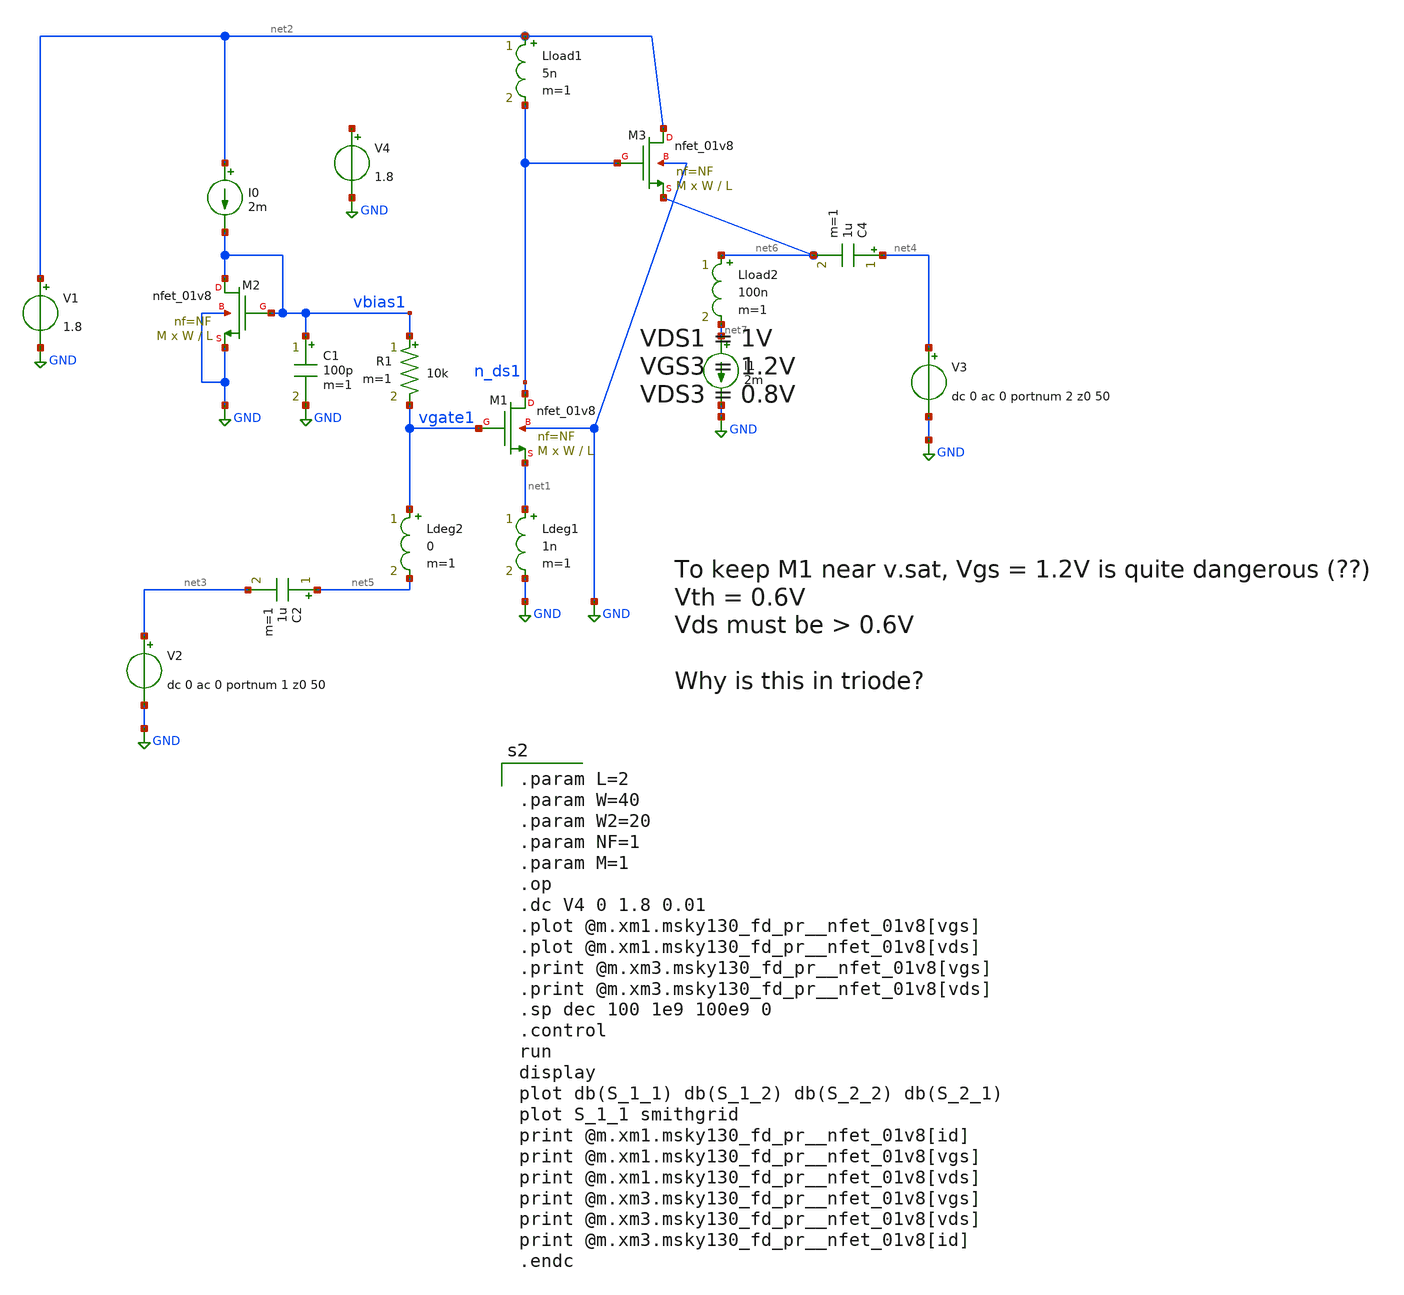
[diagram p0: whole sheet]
** sch_path: xschem/LNAs.sch
**.subckt LNAs
XM1 n_ds1 vgate1 net1 GND sky130_fd_pr__nfet_01v8 L=L W=W nf=NF ad='int((nf+1)/2) * W/nf * 0.29' as='int((nf+2)/2) * W/nf * 0.29'
+ pd='2*int((nf+1)/2) * (W/nf + 0.29)' ps='2*int((nf+2)/2) * (W/nf + 0.29)' nrd='0.29 / W' nrs='0.29 / W'
+ sa=0 sb=0 sd=0 mult=M m=M
Ldeg1 net1 GND 1n m=1
V1 net2 GND 1.8
V2 net3 GND dc 0 ac 0 portnum 1 z0 50
C2 net5 net3 1u m=1
V3 net4 GND dc 0 ac 0 portnum 2 z0 50
C4 net4 net6 1u m=1
Ldeg2 vgate1 net5 0 m=1
XM2 vbias1 vbias1 GND GND sky130_fd_pr__nfet_01v8 L=L W=W nf=NF ad='int((nf+1)/2) * W/nf * 0.29' as='int((nf+2)/2) * W/nf * 0.29'
+ pd='2*int((nf+1)/2) * (W/nf + 0.29)' ps='2*int((nf+2)/2) * (W/nf + 0.29)' nrd='0.29 / W' nrs='0.29 / W'
+ sa=0 sb=0 sd=0 mult=M m=M
R1 vbias1 vgate1 10k m=1
C1 vbias1 GND 100p m=1
I0 net2 vbias1 2m
Lload1 net2 n_ds1 5n m=1
V4 net8 GND 1.8
XM3 net2 n_ds1 net6 GND sky130_fd_pr__nfet_01v8 L=L W=W nf=NF ad='int((nf+1)/2) * W/nf * 0.29' as='int((nf+2)/2) * W/nf * 0.29'
+ pd='2*int((nf+1)/2) * (W/nf + 0.29)' ps='2*int((nf+2)/2) * (W/nf + 0.29)' nrd='0.29 / W' nrs='0.29 / W'
+ sa=0 sb=0 sd=0 mult=M m=M
I1 net7 GND 2m
Lload2 net6 net7 100n m=1
**** begin user architecture code
.lib $::SKYWATER_MODELS/sky130.lib.spice tt
.include $::PDKPATH/libs.ref/sky130_fd_sc_hvl/spice/sky130_fd_sc_hvl.spice

.param L=2
.param W=40
.param W2=20
.param NF=1
.param M=1
.op
.dc V4 0 1.8 0.01
.plot @m.xm1.msky130_fd_pr__nfet_01v8[vgs]
.plot @m.xm1.msky130_fd_pr__nfet_01v8[vds]
.print @m.xm3.msky130_fd_pr__nfet_01v8[vgs]
.print @m.xm3.msky130_fd_pr__nfet_01v8[vds]
.sp dec 100 1e9 100e9 0
.control
run
display
plot db(S_1_1) db(S_1_2) db(S_2_2) db(S_2_1)
plot S_1_1 smithgrid
print @m.xm1.msky130_fd_pr__nfet_01v8[id]
print @m.xm1.msky130_fd_pr__nfet_01v8[vgs]
print @m.xm1.msky130_fd_pr__nfet_01v8[vds]
print @m.xm3.msky130_fd_pr__nfet_01v8[vgs]
print @m.xm3.msky130_fd_pr__nfet_01v8[vds]
print @m.xm3.msky130_fd_pr__nfet_01v8[id]
.endc


**** end user architecture code
**.ends
.GLOBAL GND
.end
